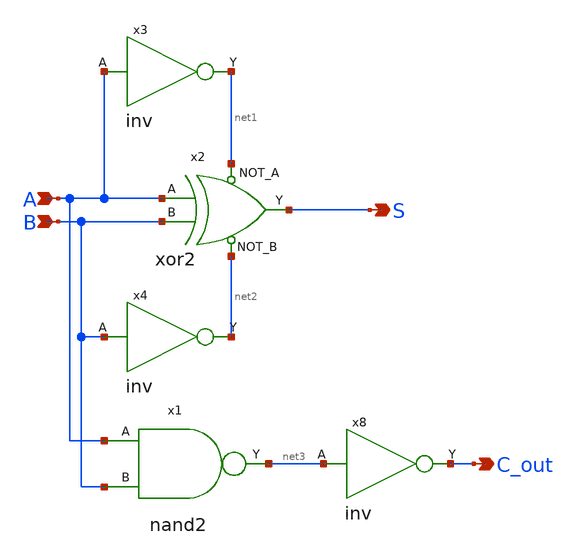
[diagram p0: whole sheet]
** sch_path: library/xschem/half_adder.sch
**.subckt half_adder S A B C_out
*.opin S
*.ipin A
*.ipin B
*.opin C_out
x2 A B net1 net2 S xor2
x3 A net1 inv
x4 B net2 inv
x1 A net3 B nand2
x8 net3 C_out inv
**.ends

* expanding   symbol:  xor2.sym # of pins=5
** sym_path: library/xschem/xor2.sym
** sch_path: library/xschem/xor2.sch
.subckt xor2 A B NOT_A NOT_B Y
*.opin Y
*.ipin A
*.ipin B
*.ipin NOT_A
*.ipin NOT_B
XM1 Y NOT_B net2 GND sky130_fd_pr__nfet_01v8 L=0.15 W=1 nf=1 ad='int((nf+1)/2) * W/nf * 0.29' as='int((nf+2)/2) * W/nf * 0.29'
+ pd='2*int((nf+1)/2) * (W/nf + 0.29)' ps='2*int((nf+2)/2) * (W/nf + 0.29)' nrd='0.29 / W' nrs='0.29 / W'
+ sa=0 sb=0 sd=0 mult=1 m=1
XM2 net1 A VDD VDD sky130_fd_pr__pfet_01v8 L=0.15 W=1 nf=1 ad='int((nf+1)/2) * W/nf * 0.29' as='int((nf+2)/2) * W/nf * 0.29'
+ pd='2*int((nf+1)/2) * (W/nf + 0.29)' ps='2*int((nf+2)/2) * (W/nf + 0.29)' nrd='0.29 / W' nrs='0.29 / W'
+ sa=0 sb=0 sd=0 mult=1 m=1
XM4 net2 NOT_A GND GND sky130_fd_pr__nfet_01v8 L=0.15 W=1 nf=1 ad='int((nf+1)/2) * W/nf * 0.29' as='int((nf+2)/2) * W/nf * 0.29'
+ pd='2*int((nf+1)/2) * (W/nf + 0.29)' ps='2*int((nf+2)/2) * (W/nf + 0.29)' nrd='0.29 / W' nrs='0.29 / W'
+ sa=0 sb=0 sd=0 mult=1 m=1
XM3 net1 B VDD VDD sky130_fd_pr__pfet_01v8 L=0.15 W=1 nf=1 ad='int((nf+1)/2) * W/nf * 0.29' as='int((nf+2)/2) * W/nf * 0.29'
+ pd='2*int((nf+1)/2) * (W/nf + 0.29)' ps='2*int((nf+2)/2) * (W/nf + 0.29)' nrd='0.29 / W' nrs='0.29 / W'
+ sa=0 sb=0 sd=0 mult=1 m=1
XM5 Y NOT_B net1 VDD sky130_fd_pr__pfet_01v8 L=0.15 W=1 nf=1 ad='int((nf+1)/2) * W/nf * 0.29' as='int((nf+2)/2) * W/nf * 0.29'
+ pd='2*int((nf+1)/2) * (W/nf + 0.29)' ps='2*int((nf+2)/2) * (W/nf + 0.29)' nrd='0.29 / W' nrs='0.29 / W'
+ sa=0 sb=0 sd=0 mult=1 m=1
XM6 Y NOT_A net1 VDD sky130_fd_pr__pfet_01v8 L=0.15 W=1 nf=1 ad='int((nf+1)/2) * W/nf * 0.29' as='int((nf+2)/2) * W/nf * 0.29'
+ pd='2*int((nf+1)/2) * (W/nf + 0.29)' ps='2*int((nf+2)/2) * (W/nf + 0.29)' nrd='0.29 / W' nrs='0.29 / W'
+ sa=0 sb=0 sd=0 mult=1 m=1
XM7 Y A net3 GND sky130_fd_pr__nfet_01v8 L=0.15 W=1 nf=1 ad='int((nf+1)/2) * W/nf * 0.29' as='int((nf+2)/2) * W/nf * 0.29'
+ pd='2*int((nf+1)/2) * (W/nf + 0.29)' ps='2*int((nf+2)/2) * (W/nf + 0.29)' nrd='0.29 / W' nrs='0.29 / W'
+ sa=0 sb=0 sd=0 mult=1 m=1
XM8 net3 B GND GND sky130_fd_pr__nfet_01v8 L=0.15 W=1 nf=1 ad='int((nf+1)/2) * W/nf * 0.29' as='int((nf+2)/2) * W/nf * 0.29'
+ pd='2*int((nf+1)/2) * (W/nf + 0.29)' ps='2*int((nf+2)/2) * (W/nf + 0.29)' nrd='0.29 / W' nrs='0.29 / W'
+ sa=0 sb=0 sd=0 mult=1 m=1
.ends


* expanding   symbol:  inv.sym # of pins=2
** sym_path: library/xschem/inv.sym
** sch_path: library/xschem/inv.sch
.subckt inv A Y
*.opin Y
*.ipin A
XM1 Y A GND GND sky130_fd_pr__nfet_01v8 L=0.15 W=1 nf=1 ad='int((nf+1)/2) * W/nf * 0.29' as='int((nf+2)/2) * W/nf * 0.29'
+ pd='2*int((nf+1)/2) * (W/nf + 0.29)' ps='2*int((nf+2)/2) * (W/nf + 0.29)' nrd='0.29 / W' nrs='0.29 / W'
+ sa=0 sb=0 sd=0 mult=1 m=1
XM2 Y A VDD VDD sky130_fd_pr__pfet_01v8 L=0.15 W=1 nf=1 ad='int((nf+1)/2) * W/nf * 0.29' as='int((nf+2)/2) * W/nf * 0.29'
+ pd='2*int((nf+1)/2) * (W/nf + 0.29)' ps='2*int((nf+2)/2) * (W/nf + 0.29)' nrd='0.29 / W' nrs='0.29 / W'
+ sa=0 sb=0 sd=0 mult=1 m=1
.ends


* expanding   symbol:  nand2.sym # of pins=3
** sym_path: library/xschem/nand2.sym
** sch_path: library/xschem/nand2.sch
.subckt nand2 A Y B
*.opin Y
*.ipin A
*.ipin B
XM1 Y B net1 GND sky130_fd_pr__nfet_01v8 L=0.15 W=1 nf=1 ad='int((nf+1)/2) * W/nf * 0.29' as='int((nf+2)/2) * W/nf * 0.29'
+ pd='2*int((nf+1)/2) * (W/nf + 0.29)' ps='2*int((nf+2)/2) * (W/nf + 0.29)' nrd='0.29 / W' nrs='0.29 / W'
+ sa=0 sb=0 sd=0 mult=1 m=1
XM2 Y B VDD VDD sky130_fd_pr__pfet_01v8 L=0.15 W=1 nf=1 ad='int((nf+1)/2) * W/nf * 0.29' as='int((nf+2)/2) * W/nf * 0.29'
+ pd='2*int((nf+1)/2) * (W/nf + 0.29)' ps='2*int((nf+2)/2) * (W/nf + 0.29)' nrd='0.29 / W' nrs='0.29 / W'
+ sa=0 sb=0 sd=0 mult=1 m=1
XM3 Y A VDD VDD sky130_fd_pr__pfet_01v8 L=0.15 W=1 nf=1 ad='int((nf+1)/2) * W/nf * 0.29' as='int((nf+2)/2) * W/nf * 0.29'
+ pd='2*int((nf+1)/2) * (W/nf + 0.29)' ps='2*int((nf+2)/2) * (W/nf + 0.29)' nrd='0.29 / W' nrs='0.29 / W'
+ sa=0 sb=0 sd=0 mult=1 m=1
XM4 net1 A GND GND sky130_fd_pr__nfet_01v8 L=0.15 W=1 nf=1 ad='int((nf+1)/2) * W/nf * 0.29' as='int((nf+2)/2) * W/nf * 0.29'
+ pd='2*int((nf+1)/2) * (W/nf + 0.29)' ps='2*int((nf+2)/2) * (W/nf + 0.29)' nrd='0.29 / W' nrs='0.29 / W'
+ sa=0 sb=0 sd=0 mult=1 m=1
.ends

.GLOBAL VDD
.GLOBAL GND
.end
